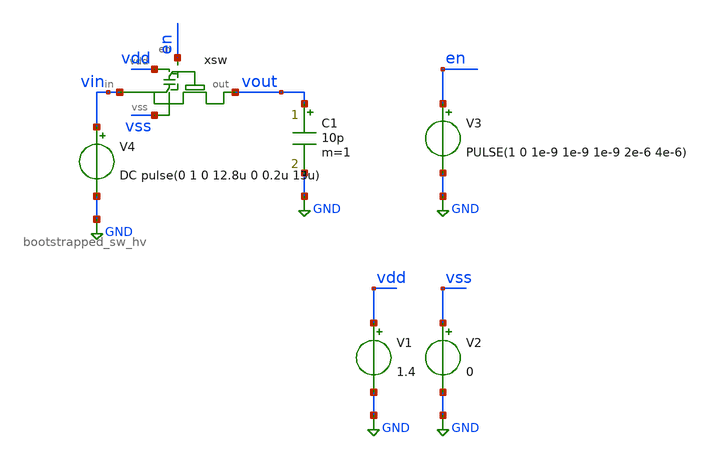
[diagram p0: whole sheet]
** sch_path: xschem/adc/tb_bootstrapped_sw.sch
**.subckt tb_bootstrapped_sw
xsw vout en vdd vin vss bootstrapped_sw_hv
V1 vdd GND 1.4
V2 vss GND 0
V3 en GND PULSE(1 0 1e-9 1e-9 1e-9 2e-6 4e-6)
C1 vout GND 10p m=1
V4 vin GND DC pulse(0 1 0 12.8u 0 0.2u 13u)
**** begin user architecture code

*.options method trap
*.options gmin 1e-15
*.options abstol 1e-15
*.options reltol 0.0001
*.options vntol 0.1e-6
*
*.include \$::DESIGN_PATH\/switches/bootstrapped_sw.sp

*.param vin=0.7
.param MC_SWITCH=0

*.tran 100e-9 12e-6
.temp 85

.control
save all
tran 100e-9 12e-6
run


* settle values
* meas tran vset find v(vout) at=3.99e-6
* meas tran vg_end find v(xsw.vg) at=3.99e-6
* meas tran vin_end find v(vin) at=3.99e-6

*let vgs_end=vg_end-vin_end

* max values
* meas tran vg_max max xsw.vg
* meas tran vs_max max xsw.vs
* meas tran vbsl_max max xsw.vbsl
* meas tran vbsh_max max xsw.vbsh

* min values
* meas tran vg_min min xsw.vg
* meas tran vs_min min xsw.vs
* meas tran vbsl_min min xsw.vbsl
* meas tran vbsh_min min xsw.vbsh


* print results
* print vset
* print vgs_end

* print vg_max
* print vs_max
* print vbsl_max
* print vbsh_max
* print vg_min
* print vs_min
* print vbsl_min
* print vbsh_min

.endc


 .lib $::SKYWATER_MODELS/sky130.lib.spice tt
.include $::SKYWATER_STDCELLS/sky130_fd_sc_hd.spice

**** end user architecture code
**.ends
.GLOBAL GND
.end
